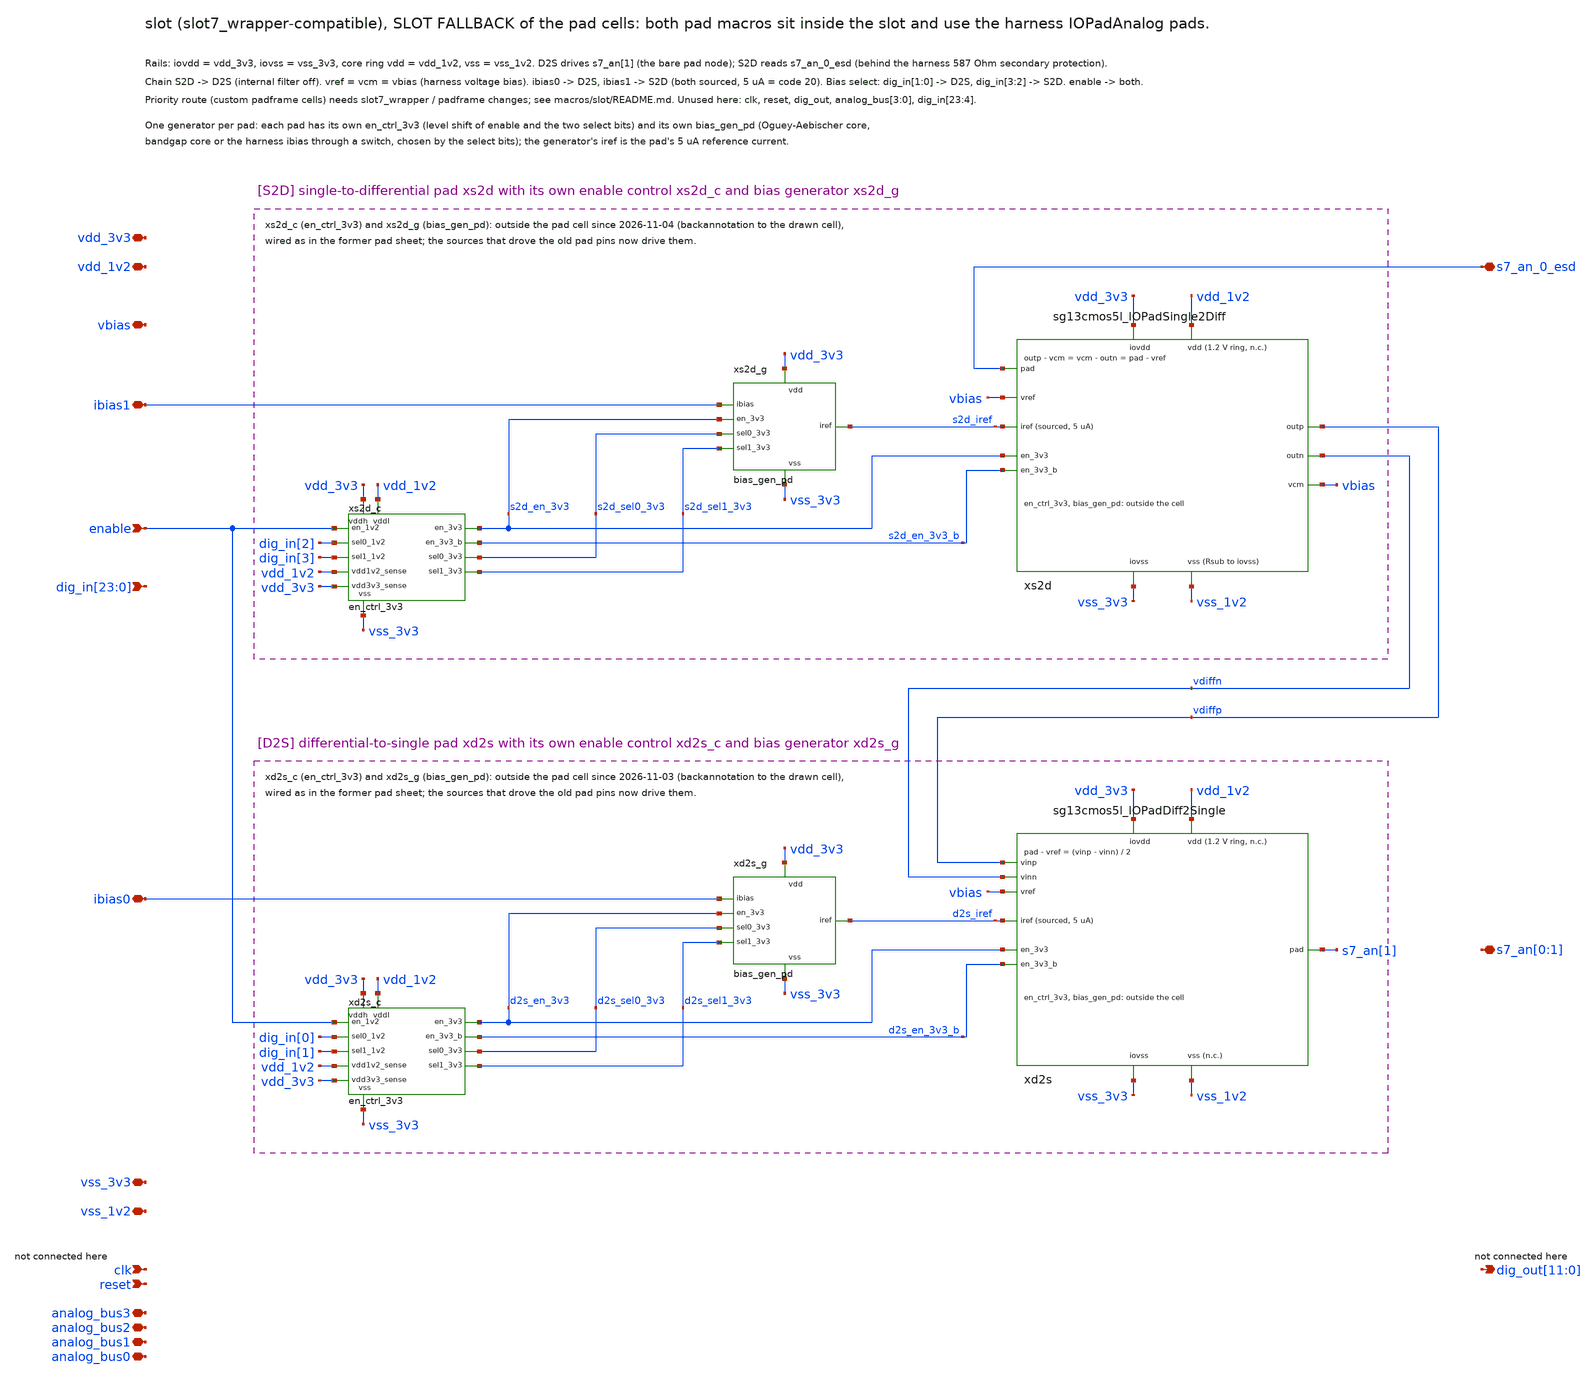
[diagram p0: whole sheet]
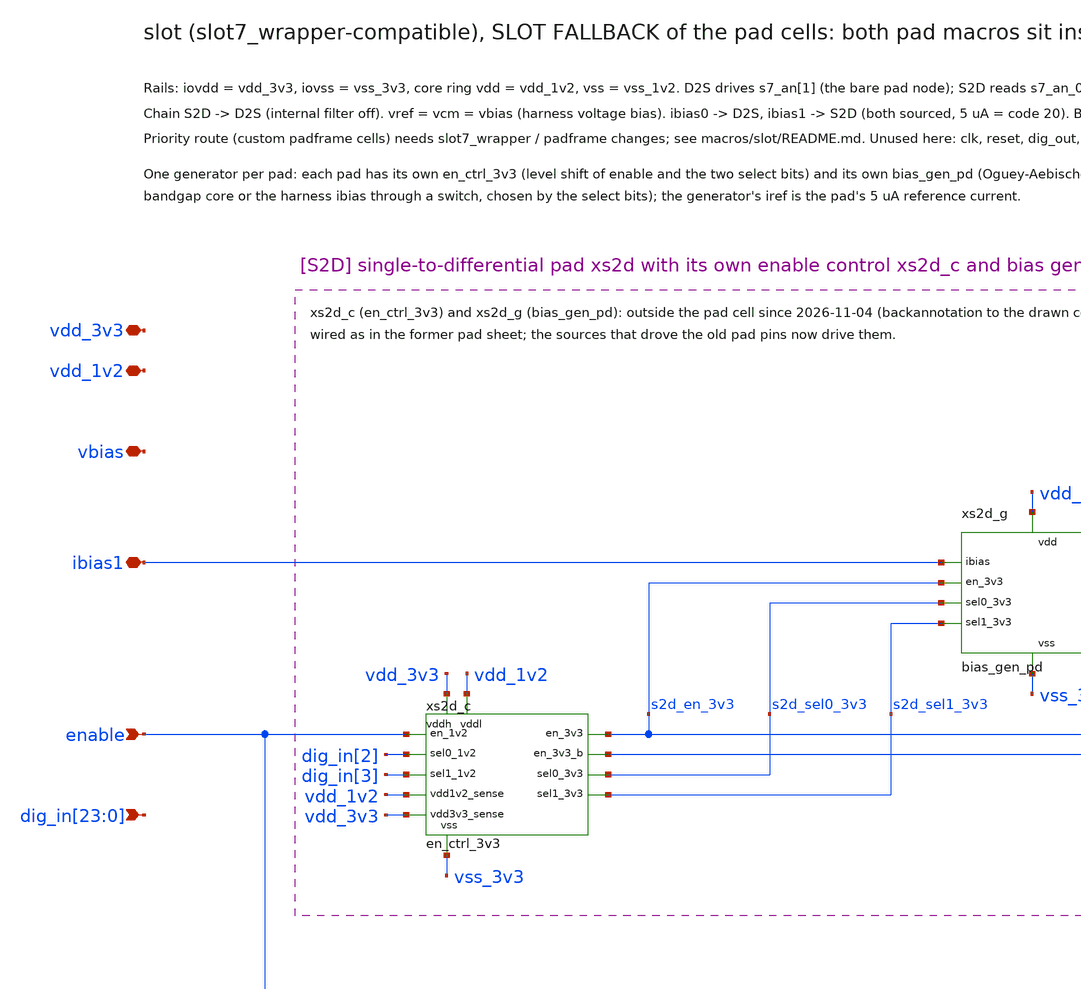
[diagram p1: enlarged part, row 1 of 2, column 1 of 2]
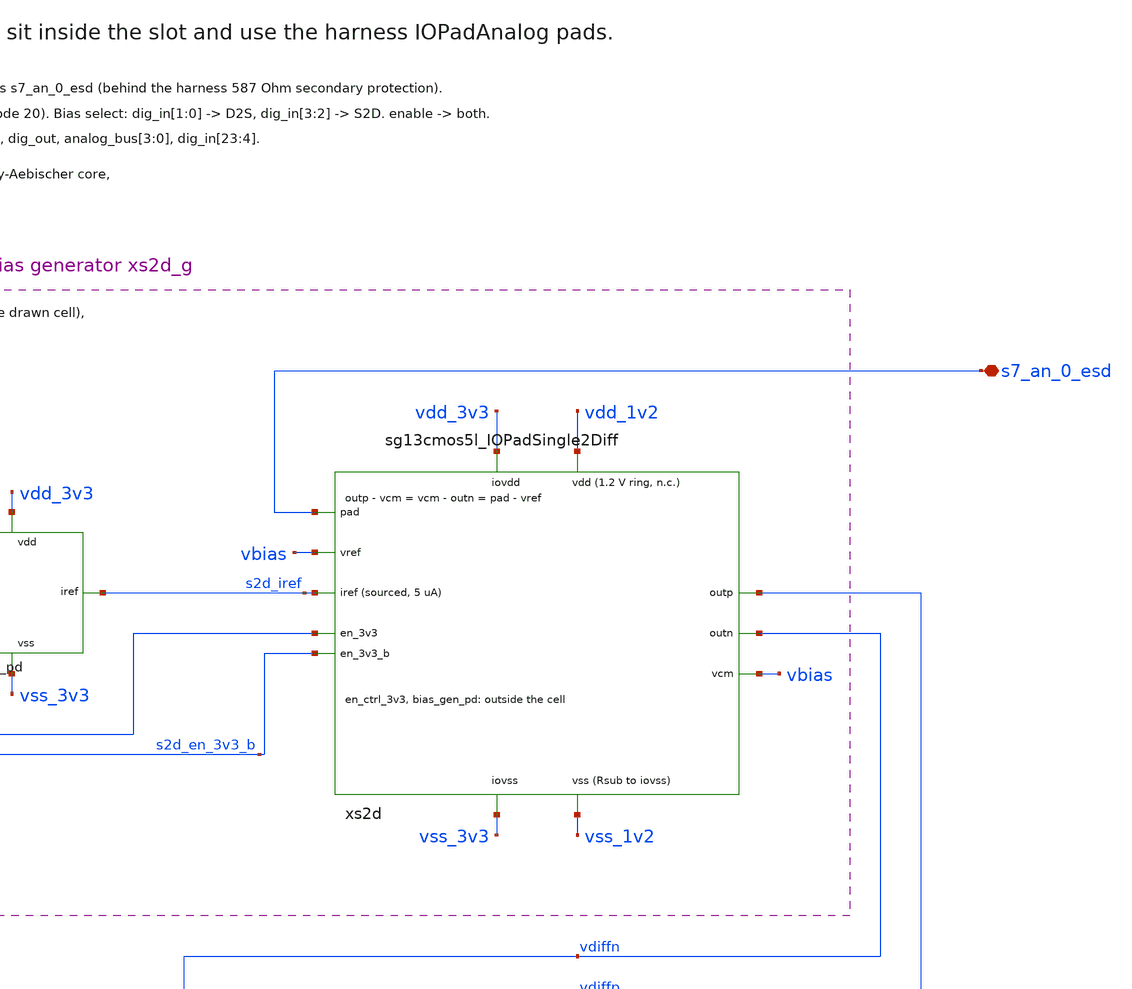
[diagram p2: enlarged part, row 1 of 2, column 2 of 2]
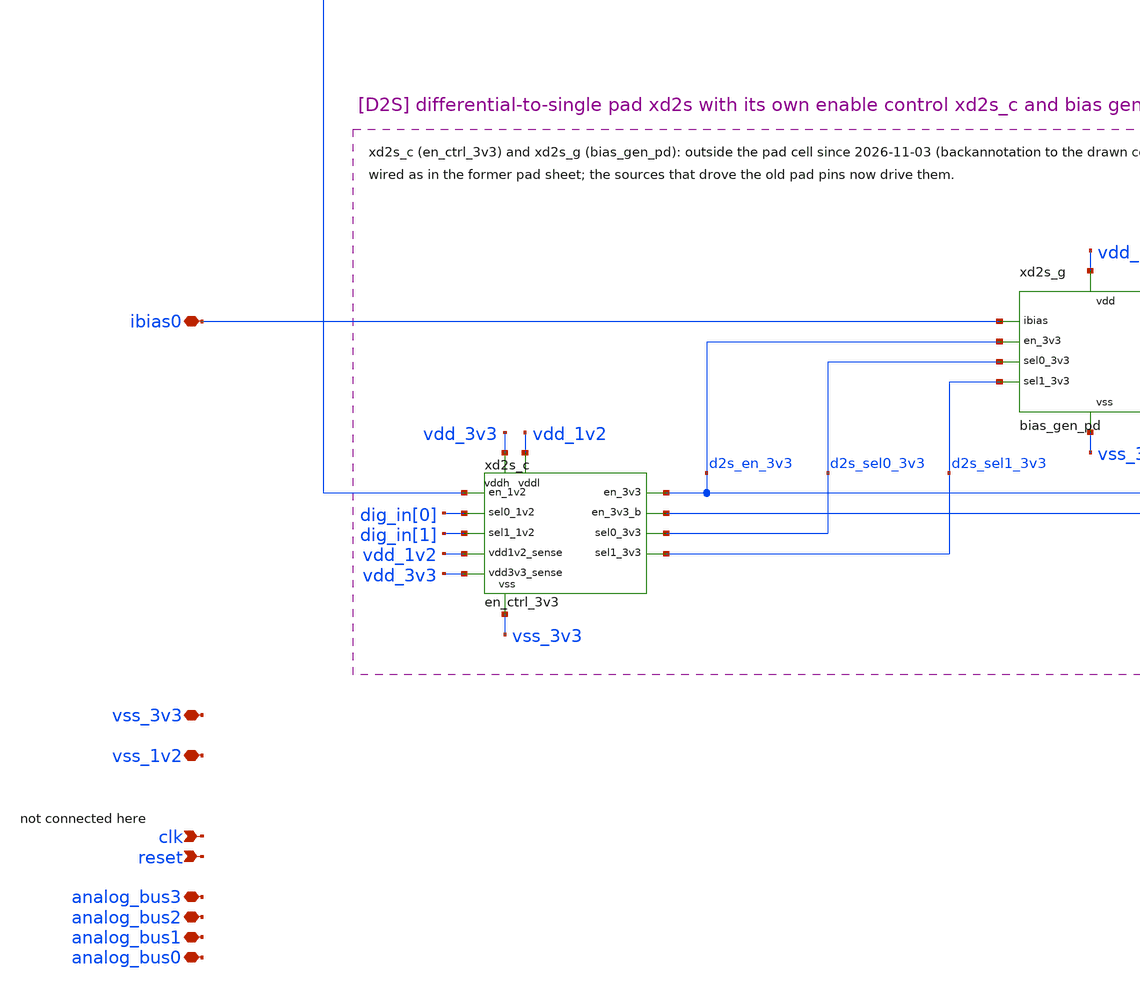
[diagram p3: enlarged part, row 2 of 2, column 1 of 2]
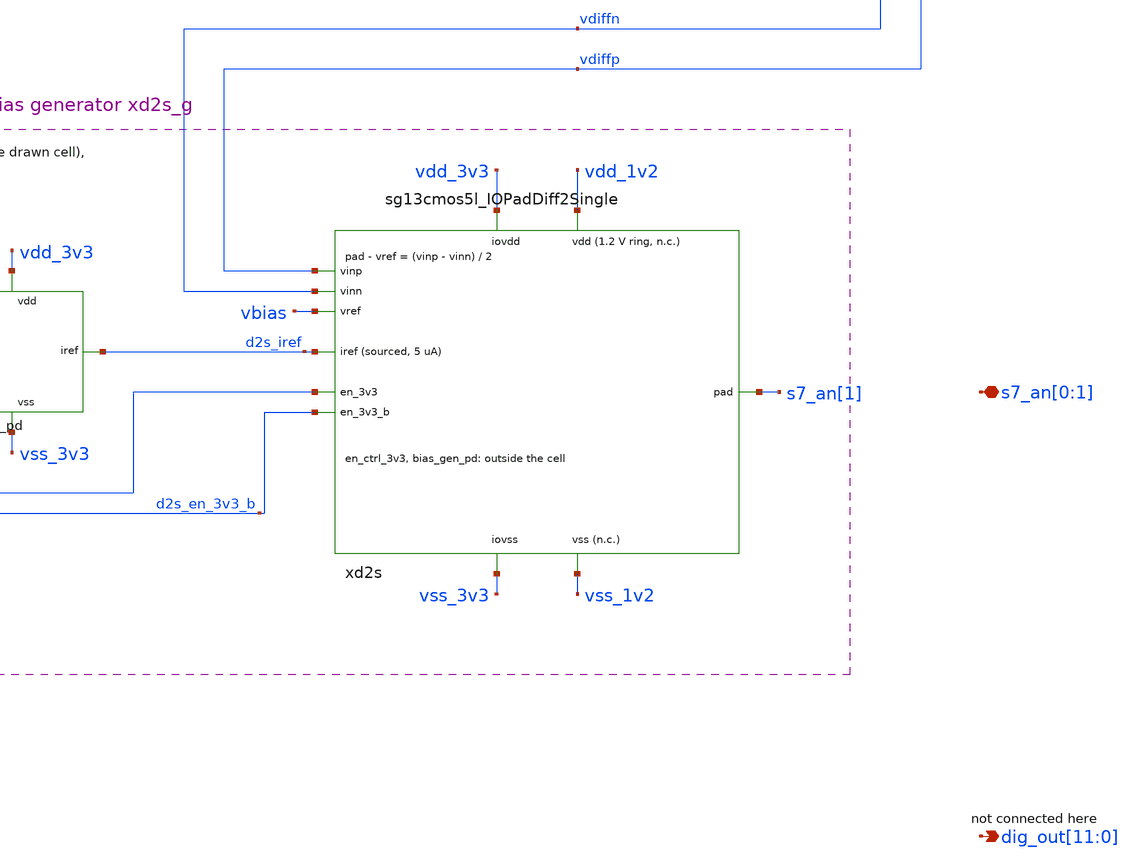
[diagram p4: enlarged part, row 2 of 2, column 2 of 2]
** sch_path: macros/slot/schematic/xschem/slot.sch
**.subckt slot
*+ dig_in[23],dig_in[22],dig_in[21],dig_in[20],dig_in[19],dig_in[18],dig_in[17],dig_in[16],dig_in[15],dig_in[14],dig_in[13],dig_in[12],dig_in[11],dig_in[10],dig_in[9],dig_in[8],dig_in[7],dig_in[6],dig_in[5],dig_in[4],dig_in[3],dig_in[2],dig_in[1],dig_in[0] enable clk reset
*+ dig_out[11],dig_out[10],dig_out[9],dig_out[8],dig_out[7],dig_out[6],dig_out[5],dig_out[4],dig_out[3],dig_out[2],dig_out[1],dig_out[0] vss_1v2 s7_an[0],s7_an[1] s7_an_0_esd vbias ibias0 ibias1 analog_bus3 analog_bus2 analog_bus1
*+ analog_bus0 vdd_1v2 vss_3v3 vdd_3v3
*.ipin
*+ dig_in[23],dig_in[22],dig_in[21],dig_in[20],dig_in[19],dig_in[18],dig_in[17],dig_in[16],dig_in[15],dig_in[14],dig_in[13],dig_in[12],dig_in[11],dig_in[10],dig_in[9],dig_in[8],dig_in[7],dig_in[6],dig_in[5],dig_in[4],dig_in[3],dig_in[2],dig_in[1],dig_in[0]
*.ipin enable
*.ipin clk
*.ipin reset
*.opin
*+ dig_out[11],dig_out[10],dig_out[9],dig_out[8],dig_out[7],dig_out[6],dig_out[5],dig_out[4],dig_out[3],dig_out[2],dig_out[1],dig_out[0]
*.iopin vss_1v2
*.iopin s7_an[0],s7_an[1]
*.iopin s7_an_0_esd
*.iopin vbias
*.iopin ibias0
*.iopin ibias1
*.iopin analog_bus3
*.iopin analog_bus2
*.iopin analog_bus1
*.iopin analog_bus0
*.iopin vdd_1v2
*.iopin vss_3v3
*.iopin vdd_3v3
xs2d vdd_3v3 vss_3v3 vdd_1v2 vss_1v2 s7_an_0_esd vdiffp vdiffn vbias vbias s2d_iref s2d_en_3v3
+ s2d_en_3v3_b sg13cmos5l_IOPadSingle2Diff
xd2s vdd_3v3 vss_3v3 vdd_1v2 vss_1v2 s7_an[1] vdiffp vdiffn vbias d2s_iref d2s_en_3v3 d2s_en_3v3_b
+ sg13cmos5l_IOPadDiff2Single
xd2s_c vdd_3v3 vdd_1v2 vss_3v3 enable dig_in[0] dig_in[1] vdd_1v2 vdd_3v3 d2s_en_3v3 d2s_sel0_3v3
+ d2s_sel1_3v3 d2s_en_3v3_b en_ctrl_3v3
xd2s_g vdd_3v3 vss_3v3 ibias0 d2s_iref d2s_en_3v3 d2s_sel0_3v3 d2s_sel1_3v3 bias_gen_pd
xs2d_c vdd_3v3 vdd_1v2 vss_3v3 enable dig_in[2] dig_in[3] vdd_1v2 vdd_3v3 s2d_en_3v3 s2d_sel0_3v3
+ s2d_sel1_3v3 s2d_en_3v3_b en_ctrl_3v3
xs2d_g vdd_3v3 vss_3v3 ibias1 s2d_iref s2d_en_3v3 s2d_sel0_3v3 s2d_sel1_3v3 bias_gen_pd
**.ends
.end
